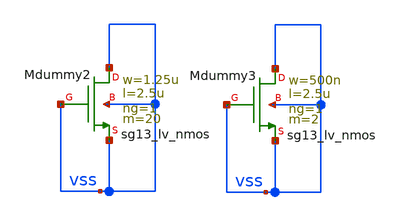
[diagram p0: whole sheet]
** sch_path: v2_feature_extr_withf/current_mirror_100x_dummy_dev.sch
**.subckt current_mirror_100x_dummy_dev
XMdummy2 vss vss vss vss sg13_lv_nmos w=1.25u l=2.5u ng=1 m=20 mm_ok=1
XMdummy3 vss vss vss vss sg13_lv_nmos w=500n l=2.5u ng=1 m=2 mm_ok=1
**.ends
.end
